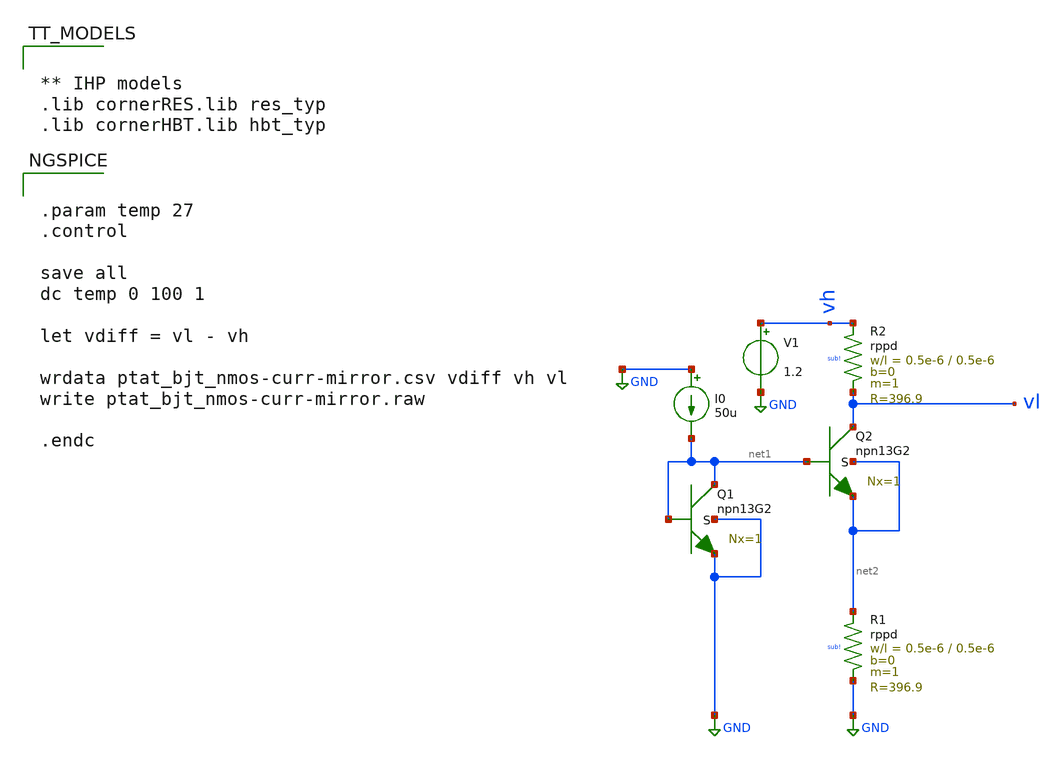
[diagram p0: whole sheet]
** sch_path: TempSensor/design_data/xschem/snoa748c_temp_sensor_tb.sch
**.subckt snoa748c_temp_sensor_tb
XQ1 net1 net1 GND GND npn13G2 Nx=1 mm_ok=1
XQ2 vl net1 net2 net2 npn13G2 Nx=1 mm_ok=1
I0 GND net1 50u
V1 vh GND 1.2
XR1 net2 GND sub! rppd w=0.5e-6 l=0.5e-6 m=1 b=0 mm_ok=1
XR2 vh vl sub! rppd w=0.5e-6 l=0.5e-6 m=1 b=0 mm_ok=1
**** begin user architecture code


.param temp 27
.control

save all
dc temp 0 100 1

let vdiff = vl - vh

wrdata ptat_bjt_nmos-curr-mirror.csv vdiff vh vl
write ptat_bjt_nmos-curr-mirror.raw

.endc




** IHP models
.lib cornerRES.lib res_typ
.lib cornerHBT.lib hbt_typ


**** end user architecture code
**.ends
.GLOBAL GND
.end
